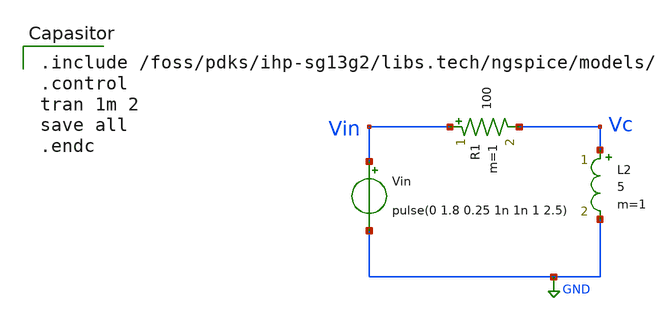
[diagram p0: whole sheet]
** sch_path: content/simulation_files/xschem/03_Inductor.sch
**.subckt 03_Inductor
Vin Vin GND pulse(0 1.8 0.25 1n 1n 1 2.5)
R1 Vin Vc 100 m=1
L2 Vc GND 5 m=1
**** begin user architecture code

.include /foss/pdks/ihp-sg13g2/libs.tech/ngspice/models/
.control
tran 1m 2
save all
.endc

**** end user architecture code
**.ends
.GLOBAL GND
.end
